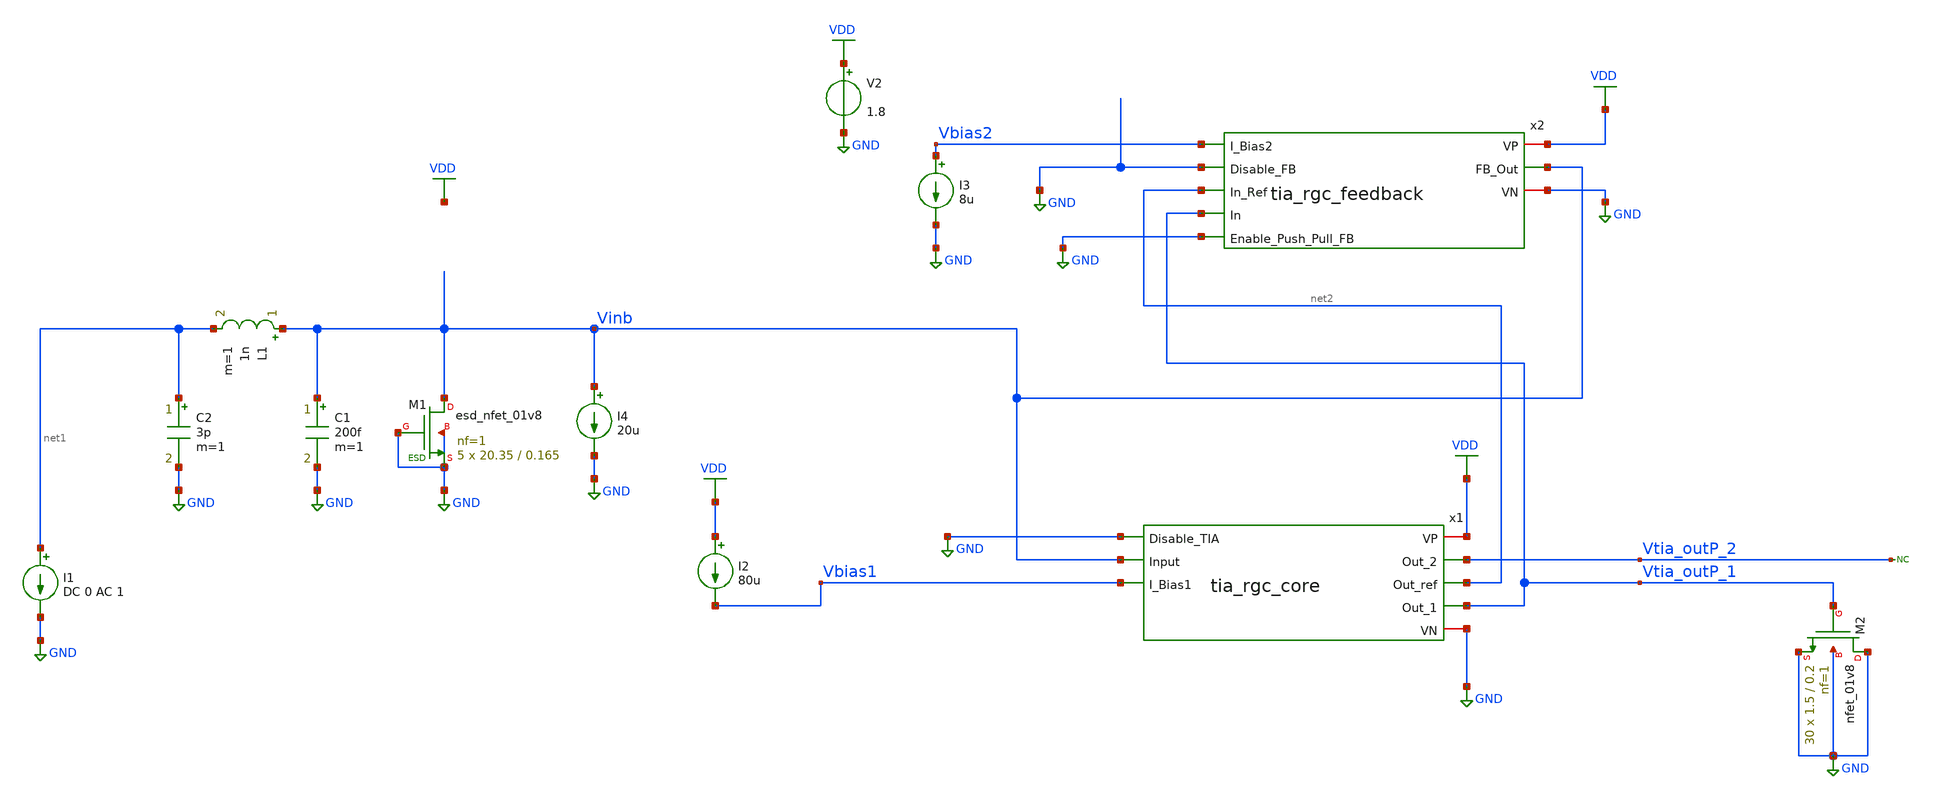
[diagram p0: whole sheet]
** sch_path: xschem/test/test_tia_rgc_full.sch
**.subckt test_tia_rgc_full
V2 VDD GND 1.8
I1 net1 GND DC 0 AC 1
I2 VDD Vbias1 80u
C1 Vinb GND 200f m=1
L1 Vinb net1 1n m=1
C2 net1 GND 3p m=1
XM1 Vinb GND GND GND sky130_fd_pr__esd_nfet_01v8 L=0.165 W=20.35 nf=1 ad='int((nf+1)/2) * W/nf * 0.29'
+ as='int((nf+2)/2) * W/nf * 0.29' pd='2*int((nf+1)/2) * (W/nf + 0.29)' ps='2*int((nf+2)/2) * (W/nf + 0.29)'
+ nrd='0.29 / W' nrs='0.29 / W' sa=0 sb=0 sd=0 mult=5 m=5
I3 Vbias2 GND 8u
XM2 GND Vtia_outP_1 GND GND sky130_fd_pr__nfet_01v8 L=0.2 W=1.5 nf=1 ad='int((nf+1)/2) * W/nf * 0.29'
+ as='int((nf+2)/2) * W/nf * 0.29' pd='2*int((nf+1)/2) * (W/nf + 0.29)' ps='2*int((nf+2)/2) * (W/nf + 0.29)'
+ nrd='0.29 / W' nrs='0.29 / W' sa=0 sb=0 sd=0 mult=30 m=30
x1 VDD Vtia_outP_2 net2 Vtia_outP_1 GND Vinb Vbias1 GND tia_rgc_core
x2 VDD Vbias2 Vinb GND net2 Vtia_outP_1 GND GND tia_rgc_feedback
* noconn Vtia_outP_2
I4 Vinb GND 20u
**** begin user architecture code


*.options savecurrents
.option warn=1
* .option temp=100
.control
set wr_vecnames
set wr_singlescale
set hcopydevtype=svg
** TIA


op
write test_tia_rgc_full.raw
run
reset
* option temp=20
* noise v(Vtia_outP-Vtia_outN) iin dec 100 1 100G
* print all
* setplot noise2
* write noise_tia2.raw
* wrdata result_noise_tia2.csv
* run
* reset

ac dec 1000 10 1T
plot vdb(Vtia_outP_1) vdb(Vtia_outP_2)
plot v(Vinb)
plot phase(Vinb)/pi*180 phase(Vtia_outP_1)/pi*180
hardcopy bandwidth.svg vdb(Vtia_outP_1)
hardcopy impedance.svg v(Vinb)


* tran 1p 100n
* plot v(Vtia_outP_1) v(Vtia_outP_2)
* plot v(Vinb)
meas ac gain FIND vdb(vtia_outp_1) AT=10MEG
meas ac max_gain max vdb(vtia_outp_1) from=1MEG to=100G
meas ac min_gain min vdb(vtia_outp_1) from=1MEG to=100MEG
let bw_gain=gain-3
meas ac bandwidth when vdb(vtia_outp_1)=bw_gain fall = LAST
wrdata result_freq.csv gain max_gain min_gain bandwidth
run
reset
noise v(vtia_outp_1) i1 dec 1000 10 2G
print all
* wrdata result_noise.csv inoise_total onoise_total
setplot noise1
plot inoise_spectrum
plot onoise_spectrum
hardcopy tia_rgc_inoise_spectrum.svg inoise_spectrum
hardcopy tia_rgc_onoise_spectrum.svg onoise_spectrum
* plot log(inoise_spectrum)
* write noise_tia2.raw
run
*
reset
noise v(vtia_outp_1) i1 dec 1000 2MEG 2G
print all
* wrdata result_noise.csv inoise_total onoise_total
setplot noise3
plot inoise_spectrum
plot onoise_spectrum
hardcopy tia_rgc_inoise_spectrum_zoom.svg inoise_spectrum
hardcopy tia_rgc_onoise_spectrum_zoom.svg onoise_spectrum
* plot log(inoise_spectrum)
* write noise_tia2.raw
run
*


.endc




* .include ../../tia.spice
* .include ../../filter_diff.spice
* .include ../../cmm_sense3.spice

.include tia_rgc_core.spice
.include tia_rgc_feedback.spice



* .lib $::SKYWATER_MODELS/sky130.lib.spice #model#
* .lib $::SKYWATER_MODELS/sky130.lib.spice sf
.lib $::SKYWATER_MODELS/sky130.lib.spice.tt.red tt
* .lib /home/simon/share/pdk/sky130A/libs.tech/ngspice/sky130.lib.spice.tt.red tt

**** end user architecture code
**.ends

* expanding   symbol:  /home/simon/code/asic/analog/tia/tia_rgc_core.sym # of pins=8
** sym_path: xschem/tia/tia_rgc_core.sym
** sch_path: xschem/tia/tia_rgc_core.sch
.subckt tia_rgc_core VP Out_2 Out_ref Out_1 Disable_TIA Input I_Bias1 VN
*.iopin VN
*.iopin VP
*.opin Out_2
*.ipin I_Bias1
*.ipin Input
*.ipin Disable_TIA
*.opin Out_1
*.opin Out_ref
XM5 VM5D I_Bias1 VN VN sky130_fd_pr__nfet_01v8 L=1 W=2 nf=1 ad='int((nf+1)/2) * W/nf * 0.29' as='int((nf+2)/2) * W/nf * 0.29'
+ pd='2*int((nf+1)/2) * (W/nf + 0.29)' ps='2*int((nf+2)/2) * (W/nf + 0.29)' nrd='0.29 / W' nrs='0.29 / W'
+ sa=0 sb=0 sd=0 mult=6 m=6
XM6 VM6D I_Bias1 VN VN sky130_fd_pr__nfet_01v8 L=1.0 W=2 nf=1 ad='int((nf+1)/2) * W/nf * 0.29' as='int((nf+2)/2) * W/nf * 0.29'
+ pd='2*int((nf+1)/2) * (W/nf + 0.29)' ps='2*int((nf+2)/2) * (W/nf + 0.29)' nrd='0.29 / W' nrs='0.29 / W'
+ sa=0 sb=0 sd=0 mult=6 m=6
XM7 Out_1 Input VM28D VN sky130_fd_pr__nfet_01v8_lvt L=0.2 W=2 nf=1 ad='int((nf+1)/2) * W/nf * 0.29'
+ as='int((nf+2)/2) * W/nf * 0.29' pd='2*int((nf+1)/2) * (W/nf + 0.29)' ps='2*int((nf+2)/2) * (W/nf + 0.29)'
+ nrd='0.29 / W' nrs='0.29 / W' sa=0 sb=0 sd=0 mult=100 m=100
XM8 Out_1 Input VP VP sky130_fd_pr__pfet_01v8 L=0.2 W=2 nf=1 ad='int((nf+1)/2) * W/nf * 0.29' as='int((nf+2)/2) * W/nf * 0.29'
+ pd='2*int((nf+1)/2) * (W/nf + 0.29)' ps='2*int((nf+2)/2) * (W/nf + 0.29)' nrd='0.29 / W' nrs='0.29 / W'
+ sa=0 sb=0 sd=0 mult=60 m=60
XM9 Input I_Bias1 VM5D VN sky130_fd_pr__nfet_01v8 L=0.15 W=2 nf=1 ad='int((nf+1)/2) * W/nf * 0.29' as='int((nf+2)/2) * W/nf * 0.29'
+ pd='2*int((nf+1)/2) * (W/nf + 0.29)' ps='2*int((nf+2)/2) * (W/nf + 0.29)' nrd='0.29 / W' nrs='0.29 / W'
+ sa=0 sb=0 sd=0 mult=12 m=12
XM10 I_Bias1 I_Bias1 VM6D VN sky130_fd_pr__nfet_01v8 L=0.15 W=2 nf=1 ad='int((nf+1)/2) * W/nf * 0.29'
+ as='int((nf+2)/2) * W/nf * 0.29' pd='2*int((nf+1)/2) * (W/nf + 0.29)' ps='2*int((nf+2)/2) * (W/nf + 0.29)'
+ nrd='0.29 / W' nrs='0.29 / W' sa=0 sb=0 sd=0 mult=12 m=12
XM23 I_Bias1 Disable_TIA VN VN sky130_fd_pr__nfet_01v8 L=0.15 W=2 nf=1 ad='int((nf+1)/2) * W/nf * 0.29'
+ as='int((nf+2)/2) * W/nf * 0.29' pd='2*int((nf+1)/2) * (W/nf + 0.29)' ps='2*int((nf+2)/2) * (W/nf + 0.29)'
+ nrd='0.29 / W' nrs='0.29 / W' sa=0 sb=0 sd=0 mult=5 m=5
XM26 Disable_TIA_B Disable_TIA VN VN sky130_fd_pr__nfet_01v8 L=1 W=0.5 nf=1 ad='int((nf+1)/2) * W/nf * 0.29'
+ as='int((nf+2)/2) * W/nf * 0.29' pd='2*int((nf+1)/2) * (W/nf + 0.29)' ps='2*int((nf+2)/2) * (W/nf + 0.29)'
+ nrd='0.29 / W' nrs='0.29 / W' sa=0 sb=0 sd=0 mult=1 m=1
XM27 Disable_TIA_B Disable_TIA VP VP sky130_fd_pr__pfet_01v8 L=1 W=0.5 nf=1 ad='int((nf+1)/2) * W/nf * 0.29'
+ as='int((nf+2)/2) * W/nf * 0.29' pd='2*int((nf+1)/2) * (W/nf + 0.29)' ps='2*int((nf+2)/2) * (W/nf + 0.29)'
+ nrd='0.29 / W' nrs='0.29 / W' sa=0 sb=0 sd=0 mult=1 m=1
XM28 VM28D Disable_TIA_B VN VN sky130_fd_pr__nfet_01v8 L=0.15 W=2 nf=1 ad='int((nf+1)/2) * W/nf * 0.29'
+ as='int((nf+2)/2) * W/nf * 0.29' pd='2*int((nf+1)/2) * (W/nf + 0.29)' ps='2*int((nf+2)/2) * (W/nf + 0.29)'
+ nrd='0.29 / W' nrs='0.29 / W' sa=0 sb=0 sd=0 mult=100 m=100
XM36 VM36D I_Bias1 VN VN sky130_fd_pr__nfet_01v8 L=1 W=2 nf=1 ad='int((nf+1)/2) * W/nf * 0.29' as='int((nf+2)/2) * W/nf * 0.29'
+ pd='2*int((nf+1)/2) * (W/nf + 0.29)' ps='2*int((nf+2)/2) * (W/nf + 0.29)' nrd='0.29 / W' nrs='0.29 / W'
+ sa=0 sb=0 sd=0 mult=6 m=6
XM37 Out_ref VM39D VM40D VN sky130_fd_pr__nfet_01v8_lvt L=0.2 W=2 nf=1 ad='int((nf+1)/2) * W/nf * 0.29'
+ as='int((nf+2)/2) * W/nf * 0.29' pd='2*int((nf+1)/2) * (W/nf + 0.29)' ps='2*int((nf+2)/2) * (W/nf + 0.29)'
+ nrd='0.29 / W' nrs='0.29 / W' sa=0 sb=0 sd=0 mult=100 m=100
XM38 Out_ref VM39D VP VP sky130_fd_pr__pfet_01v8 L=0.2 W=2 nf=1 ad='int((nf+1)/2) * W/nf * 0.29' as='int((nf+2)/2) * W/nf * 0.29'
+ pd='2*int((nf+1)/2) * (W/nf + 0.29)' ps='2*int((nf+2)/2) * (W/nf + 0.29)' nrd='0.29 / W' nrs='0.29 / W'
+ sa=0 sb=0 sd=0 mult=60 m=60
XM39 VM39D I_Bias1 VM36D VN sky130_fd_pr__nfet_01v8 L=0.15 W=2 nf=1 ad='int((nf+1)/2) * W/nf * 0.29'
+ as='int((nf+2)/2) * W/nf * 0.29' pd='2*int((nf+1)/2) * (W/nf + 0.29)' ps='2*int((nf+2)/2) * (W/nf + 0.29)'
+ nrd='0.29 / W' nrs='0.29 / W' sa=0 sb=0 sd=0 mult=12 m=12
XM40 VM40D Disable_TIA_B VN VN sky130_fd_pr__nfet_01v8 L=0.15 W=2 nf=1 ad='int((nf+1)/2) * W/nf * 0.29'
+ as='int((nf+2)/2) * W/nf * 0.29' pd='2*int((nf+1)/2) * (W/nf + 0.29)' ps='2*int((nf+2)/2) * (W/nf + 0.29)'
+ nrd='0.29 / W' nrs='0.29 / W' sa=0 sb=0 sd=0 mult=100 m=100
XC20 VP VN sky130_fd_pr__cap_mim_m3_2 W=30 L=30 MF=1 m=1
XM16 Out_2 VN VP VP sky130_fd_pr__pfet_01v8 L=0.5 W=2 nf=1 ad='int((nf+1)/2) * W/nf * 0.29' as='int((nf+2)/2) * W/nf * 0.29'
+ pd='2*int((nf+1)/2) * (W/nf + 0.29)' ps='2*int((nf+2)/2) * (W/nf + 0.29)' nrd='0.29 / W' nrs='0.29 / W'
+ sa=0 sb=0 sd=0 mult=10 m=10
XM15 Out_2 Out_1 Input Input sky130_fd_pr__nfet_01v8_lvt L=0.2 W=2 nf=1 ad='int((nf+1)/2) * W/nf * 0.29'
+ as='int((nf+2)/2) * W/nf * 0.29' pd='2*int((nf+1)/2) * (W/nf + 0.29)' ps='2*int((nf+2)/2) * (W/nf + 0.29)'
+ nrd='0.29 / W' nrs='0.29 / W' sa=0 sb=0 sd=0 mult=30 m=30
XM31 VM31D Out_ref VM39D VM39D sky130_fd_pr__nfet_01v8_lvt L=0.2 W=2 nf=1 ad='int((nf+1)/2) * W/nf * 0.29'
+ as='int((nf+2)/2) * W/nf * 0.29' pd='2*int((nf+1)/2) * (W/nf + 0.29)' ps='2*int((nf+2)/2) * (W/nf + 0.29)'
+ nrd='0.29 / W' nrs='0.29 / W' sa=0 sb=0 sd=0 mult=30 m=30
XM35 VM31D VN VP VP sky130_fd_pr__pfet_01v8 L=0.5 W=2 nf=1 ad='int((nf+1)/2) * W/nf * 0.29' as='int((nf+2)/2) * W/nf * 0.29'
+ pd='2*int((nf+1)/2) * (W/nf + 0.29)' ps='2*int((nf+2)/2) * (W/nf + 0.29)' nrd='0.29 / W' nrs='0.29 / W'
+ sa=0 sb=0 sd=0 mult=10 m=10
XC7 VP VN sky130_fd_pr__cap_mim_m3_2 W=30 L=30 MF=1 m=1
XC2 VP VM28D sky130_fd_pr__cap_mim_m3_2 W=20 L=30 MF=1 m=1
XC5 VN I_Bias1 sky130_fd_pr__cap_mim_m3_1 W=15 L=12 MF=1 m=1
XC4 VN I_Bias1 sky130_fd_pr__cap_mim_m3_1 W=15 L=12 MF=1 m=1
XC1 VP VM40D sky130_fd_pr__cap_mim_m3_2 W=20 L=30 MF=1 m=1
XC3 Disable_TIA_B VN VN sky130_fd_pr__cap_var_lvt W=2 L=5 VM=5 m=5
.ends


* expanding   symbol:  /home/simon/code/asic/analog/tia/tia_rgc_feedback.sym # of pins=8
** sym_path: xschem/tia/tia_rgc_feedback.sym
** sch_path: xschem/tia/tia_rgc_feedback.sch
.subckt tia_rgc_feedback VP I_Bias2 FB_Out Disable_FB In_Ref In Enable_Push_Pull_FB VN
*.iopin VN
*.iopin VP
*.ipin I_Bias2
*.ipin Disable_FB
*.ipin Enable_Push_Pull_FB
*.ipin In_Ref
*.opin FB_Out
*.ipin In
XM3 net2 net1 VN VN sky130_fd_pr__nfet_01v8 L=0.5 W=2 nf=1 ad='int((nf+1)/2) * W/nf * 0.29' as='int((nf+2)/2) * W/nf * 0.29'
+ pd='2*int((nf+1)/2) * (W/nf + 0.29)' ps='2*int((nf+2)/2) * (W/nf + 0.29)' nrd='0.29 / W' nrs='0.29 / W'
+ sa=0 sb=0 sd=0 mult=1 m=1
XM4 net1 net1 net2 VN sky130_fd_pr__nfet_01v8 L=0.15 W=2 nf=1 ad='int((nf+1)/2) * W/nf * 0.29' as='int((nf+2)/2) * W/nf * 0.29'
+ pd='2*int((nf+1)/2) * (W/nf + 0.29)' ps='2*int((nf+2)/2) * (W/nf + 0.29)' nrd='0.29 / W' nrs='0.29 / W'
+ sa=0 sb=0 sd=0 mult=4 m=4
XM12 net3 net1 VN VN sky130_fd_pr__nfet_01v8 L=0.5 W=2 nf=1 ad='int((nf+1)/2) * W/nf * 0.29' as='int((nf+2)/2) * W/nf * 0.29'
+ pd='2*int((nf+1)/2) * (W/nf + 0.29)' ps='2*int((nf+2)/2) * (W/nf + 0.29)' nrd='0.29 / W' nrs='0.29 / W'
+ sa=0 sb=0 sd=0 mult=2 m=2
XM13 VM13D net1 net3 VN sky130_fd_pr__nfet_01v8 L=0.15 W=2 nf=1 ad='int((nf+1)/2) * W/nf * 0.29' as='int((nf+2)/2) * W/nf * 0.29'
+ pd='2*int((nf+1)/2) * (W/nf + 0.29)' ps='2*int((nf+2)/2) * (W/nf + 0.29)' nrd='0.29 / W' nrs='0.29 / W'
+ sa=0 sb=0 sd=0 mult=8 m=8
XM1 net5 I_Bias2 VP VP sky130_fd_pr__pfet_01v8 L=0.5 W=2 nf=1 ad='int((nf+1)/2) * W/nf * 0.29' as='int((nf+2)/2) * W/nf * 0.29'
+ pd='2*int((nf+1)/2) * (W/nf + 0.29)' ps='2*int((nf+2)/2) * (W/nf + 0.29)' nrd='0.29 / W' nrs='0.29 / W'
+ sa=0 sb=0 sd=0 mult=2 m=2
XM29 Disable_FB_B Disable_FB VN VN sky130_fd_pr__nfet_01v8 L=0.15 W=1 nf=1 ad='int((nf+1)/2) * W/nf * 0.29'
+ as='int((nf+2)/2) * W/nf * 0.29' pd='2*int((nf+1)/2) * (W/nf + 0.29)' ps='2*int((nf+2)/2) * (W/nf + 0.29)'
+ nrd='0.29 / W' nrs='0.29 / W' sa=0 sb=0 sd=0 mult=1 m=1
XM30 Disable_FB_B Disable_FB VP VP sky130_fd_pr__pfet_01v8 L=0.15 W=1 nf=1 ad='int((nf+1)/2) * W/nf * 0.29'
+ as='int((nf+2)/2) * W/nf * 0.29' pd='2*int((nf+1)/2) * (W/nf + 0.29)' ps='2*int((nf+2)/2) * (W/nf + 0.29)'
+ nrd='0.29 / W' nrs='0.29 / W' sa=0 sb=0 sd=0 mult=1 m=1
XM32 VM14D Disable_FB_B VP VP sky130_fd_pr__pfet_01v8 L=0.15 W=2 nf=1 ad='int((nf+1)/2) * W/nf * 0.29'
+ as='int((nf+2)/2) * W/nf * 0.29' pd='2*int((nf+1)/2) * (W/nf + 0.29)' ps='2*int((nf+2)/2) * (W/nf + 0.29)'
+ nrd='0.29 / W' nrs='0.29 / W' sa=0 sb=0 sd=0 mult=1 m=1
XM33 VM16D Disable_FB_B VP VP sky130_fd_pr__pfet_01v8 L=0.15 W=2 nf=1 ad='int((nf+1)/2) * W/nf * 0.29'
+ as='int((nf+2)/2) * W/nf * 0.29' pd='2*int((nf+1)/2) * (W/nf + 0.29)' ps='2*int((nf+2)/2) * (W/nf + 0.29)'
+ nrd='0.29 / W' nrs='0.29 / W' sa=0 sb=0 sd=0 mult=1 m=1
XM42 net4 net1 VN VN sky130_fd_pr__nfet_01v8 L=0.5 W=2 nf=1 ad='int((nf+1)/2) * W/nf * 0.29' as='int((nf+2)/2) * W/nf * 0.29'
+ pd='2*int((nf+1)/2) * (W/nf + 0.29)' ps='2*int((nf+2)/2) * (W/nf + 0.29)' nrd='0.29 / W' nrs='0.29 / W'
+ sa=0 sb=0 sd=0 mult=1 m=1
XM43 VM34G net1 net4 VN sky130_fd_pr__nfet_01v8 L=0.15 W=2 nf=1 ad='int((nf+1)/2) * W/nf * 0.29' as='int((nf+2)/2) * W/nf * 0.29'
+ pd='2*int((nf+1)/2) * (W/nf + 0.29)' ps='2*int((nf+2)/2) * (W/nf + 0.29)' nrd='0.29 / W' nrs='0.29 / W'
+ sa=0 sb=0 sd=0 mult=4 m=4
XM17 net1 I_Bias2 net5 VP sky130_fd_pr__pfet_01v8 L=0.15 W=2 nf=1 ad='int((nf+1)/2) * W/nf * 0.29' as='int((nf+2)/2) * W/nf * 0.29'
+ pd='2*int((nf+1)/2) * (W/nf + 0.29)' ps='2*int((nf+2)/2) * (W/nf + 0.29)' nrd='0.29 / W' nrs='0.29 / W'
+ sa=0 sb=0 sd=0 mult=8 m=8
XM2 net6 I_Bias2 VP VP sky130_fd_pr__pfet_01v8 L=0.5 W=2 nf=1 ad='int((nf+1)/2) * W/nf * 0.29' as='int((nf+2)/2) * W/nf * 0.29'
+ pd='2*int((nf+1)/2) * (W/nf + 0.29)' ps='2*int((nf+2)/2) * (W/nf + 0.29)' nrd='0.29 / W' nrs='0.29 / W'
+ sa=0 sb=0 sd=0 mult=2 m=2
XM18 VM16D I_Bias2 net6 VP sky130_fd_pr__pfet_01v8 L=0.15 W=2 nf=1 ad='int((nf+1)/2) * W/nf * 0.29' as='int((nf+2)/2) * W/nf * 0.29'
+ pd='2*int((nf+1)/2) * (W/nf + 0.29)' ps='2*int((nf+2)/2) * (W/nf + 0.29)' nrd='0.29 / W' nrs='0.29 / W'
+ sa=0 sb=0 sd=0 mult=8 m=8
XM19 net7 I_Bias2 VP VP sky130_fd_pr__pfet_01v8 L=0.5 W=2 nf=1 ad='int((nf+1)/2) * W/nf * 0.29' as='int((nf+2)/2) * W/nf * 0.29'
+ pd='2*int((nf+1)/2) * (W/nf + 0.29)' ps='2*int((nf+2)/2) * (W/nf + 0.29)' nrd='0.29 / W' nrs='0.29 / W'
+ sa=0 sb=0 sd=0 mult=2 m=2
XM20 VM14D I_Bias2 net7 VP sky130_fd_pr__pfet_01v8 L=0.15 W=2 nf=1 ad='int((nf+1)/2) * W/nf * 0.29' as='int((nf+2)/2) * W/nf * 0.29'
+ pd='2*int((nf+1)/2) * (W/nf + 0.29)' ps='2*int((nf+2)/2) * (W/nf + 0.29)' nrd='0.29 / W' nrs='0.29 / W'
+ sa=0 sb=0 sd=0 mult=8 m=8
XM34 FB_Out VM34G net10 VN sky130_fd_pr__nfet_01v8 L=0.15 W=2 nf=1 ad='int((nf+1)/2) * W/nf * 0.29' as='int((nf+2)/2) * W/nf * 0.29'
+ pd='2*int((nf+1)/2) * (W/nf + 0.29)' ps='2*int((nf+2)/2) * (W/nf + 0.29)' nrd='0.29 / W' nrs='0.29 / W'
+ sa=0 sb=0 sd=0 mult=10 m=10
XM25 FB_Out VM25G net11 VP sky130_fd_pr__pfet_01v8 L=0.15 W=2 nf=1 ad='int((nf+1)/2) * W/nf * 0.29' as='int((nf+2)/2) * W/nf * 0.29'
+ pd='2*int((nf+1)/2) * (W/nf + 0.29)' ps='2*int((nf+2)/2) * (W/nf + 0.29)' nrd='0.29 / W' nrs='0.29 / W'
+ sa=0 sb=0 sd=0 mult=20 m=20
XM45 VM25G VM25G net8 net8 sky130_fd_pr__nfet_01v8_lvt L=0.15 W=1 nf=1 ad='int((nf+1)/2) * W/nf * 0.29'
+ as='int((nf+2)/2) * W/nf * 0.29' pd='2*int((nf+1)/2) * (W/nf + 0.29)' ps='2*int((nf+2)/2) * (W/nf + 0.29)'
+ nrd='0.29 / W' nrs='0.29 / W' sa=0 sb=0 sd=0 mult=1 m=1
XM46 FB_Out VM14D VP VP sky130_fd_pr__pfet_01v8 L=0.3 W=2 nf=1 ad='int((nf+1)/2) * W/nf * 0.29' as='int((nf+2)/2) * W/nf * 0.29'
+ pd='2*int((nf+1)/2) * (W/nf + 0.29)' ps='2*int((nf+2)/2) * (W/nf + 0.29)' nrd='0.29 / W' nrs='0.29 / W'
+ sa=0 sb=0 sd=0 mult=3 m=3
XM47 net9 net1 VN VN sky130_fd_pr__nfet_01v8 L=0.5 W=2 nf=1 ad='int((nf+1)/2) * W/nf * 0.29' as='int((nf+2)/2) * W/nf * 0.29'
+ pd='2*int((nf+1)/2) * (W/nf + 0.29)' ps='2*int((nf+2)/2) * (W/nf + 0.29)' nrd='0.29 / W' nrs='0.29 / W'
+ sa=0 sb=0 sd=0 mult=3 m=3
XM48 FB_Out net1 net9 VN sky130_fd_pr__nfet_01v8 L=0.15 W=2 nf=1 ad='int((nf+1)/2) * W/nf * 0.29' as='int((nf+2)/2) * W/nf * 0.29'
+ pd='2*int((nf+1)/2) * (W/nf + 0.29)' ps='2*int((nf+2)/2) * (W/nf + 0.29)' nrd='0.29 / W' nrs='0.29 / W'
+ sa=0 sb=0 sd=0 mult=12 m=12
XC8 VP VM14D sky130_fd_pr__cap_mim_m3_2 W=20 L=20 MF=1 m=1
XM52 EN_PP_FB Enable_Push_Pull_FB VN VN sky130_fd_pr__nfet_01v8 L=0.15 W=1 nf=1 ad='int((nf+1)/2) * W/nf * 0.29'
+ as='int((nf+2)/2) * W/nf * 0.29' pd='2*int((nf+1)/2) * (W/nf + 0.29)' ps='2*int((nf+2)/2) * (W/nf + 0.29)'
+ nrd='0.29 / W' nrs='0.29 / W' sa=0 sb=0 sd=0 mult=1 m=1
XM53 EN_PP_FB Enable_Push_Pull_FB VP VP sky130_fd_pr__pfet_01v8 L=0.15 W=1 nf=1 ad='int((nf+1)/2) * W/nf * 0.29'
+ as='int((nf+2)/2) * W/nf * 0.29' pd='2*int((nf+1)/2) * (W/nf + 0.29)' ps='2*int((nf+2)/2) * (W/nf + 0.29)'
+ nrd='0.29 / W' nrs='0.29 / W' sa=0 sb=0 sd=0 mult=1 m=1
XM49 net8 Enable_Push_Pull_FB VM34G VN sky130_fd_pr__nfet_01v8_lvt L=0.15 W=1 nf=1 ad='int((nf+1)/2) * W/nf * 0.29'
+ as='int((nf+2)/2) * W/nf * 0.29' pd='2*int((nf+1)/2) * (W/nf + 0.29)' ps='2*int((nf+2)/2) * (W/nf + 0.29)'
+ nrd='0.29 / W' nrs='0.29 / W' sa=0 sb=0 sd=0 mult=1 m=1
XM50 VM34G EN_PP_FB VN VN sky130_fd_pr__nfet_01v8_lvt L=0.15 W=1 nf=1 ad='int((nf+1)/2) * W/nf * 0.29'
+ as='int((nf+2)/2) * W/nf * 0.29' pd='2*int((nf+1)/2) * (W/nf + 0.29)' ps='2*int((nf+2)/2) * (W/nf + 0.29)'
+ nrd='0.29 / W' nrs='0.29 / W' sa=0 sb=0 sd=0 mult=1 m=1
XM51 VM25G Enable_Push_Pull_FB VP VP sky130_fd_pr__pfet_01v8 L=0.15 W=1 nf=1 ad='int((nf+1)/2) * W/nf * 0.29'
+ as='int((nf+2)/2) * W/nf * 0.29' pd='2*int((nf+1)/2) * (W/nf + 0.29)' ps='2*int((nf+2)/2) * (W/nf + 0.29)'
+ nrd='0.29 / W' nrs='0.29 / W' sa=0 sb=0 sd=0 mult=1 m=1
XM44 net10 VM34G VN VN sky130_fd_pr__nfet_01v8 L=0.5 W=2 nf=1 ad='int((nf+1)/2) * W/nf * 0.29' as='int((nf+2)/2) * W/nf * 0.29'
+ pd='2*int((nf+1)/2) * (W/nf + 0.29)' ps='2*int((nf+2)/2) * (W/nf + 0.29)' nrd='0.29 / W' nrs='0.29 / W'
+ sa=0 sb=0 sd=0 mult=5 m=5
XM54 net11 VM25G VP VP sky130_fd_pr__pfet_01v8 L=0.5 W=2 nf=1 ad='int((nf+1)/2) * W/nf * 0.29' as='int((nf+2)/2) * W/nf * 0.29'
+ pd='2*int((nf+1)/2) * (W/nf + 0.29)' ps='2*int((nf+2)/2) * (W/nf + 0.29)' nrd='0.29 / W' nrs='0.29 / W'
+ sa=0 sb=0 sd=0 mult=10 m=10
XM11 VM25G VM16D VP VP sky130_fd_pr__pfet_01v8_lvt L=0.35 W=2 nf=1 ad='int((nf+1)/2) * W/nf * 0.29' as='int((nf+2)/2) * W/nf * 0.29'
+ pd='2*int((nf+1)/2) * (W/nf + 0.29)' ps='2*int((nf+2)/2) * (W/nf + 0.29)' nrd='0.29 / W' nrs='0.29 / W'
+ sa=0 sb=0 sd=0 mult=2 m=2
XC20 VP VN sky130_fd_pr__cap_mim_m3_2 W=30 L=30 MF=1 m=1
XC18 net1 VN VN sky130_fd_pr__cap_var_lvt W=3 L=3 VM=10 m=10
XC11 VM16D VN VN sky130_fd_pr__cap_var_lvt W=3 L=3 VM=20 m=20
XC12 VP VM16D sky130_fd_pr__cap_mim_m3_2 W=20 L=20 MF=1 m=1
XC22 Enable_Push_Pull_FB VN sky130_fd_pr__cap_mim_m3_2 W=20 L=20 MF=1 m=1
XM21 net12 I_Bias2 VP VP sky130_fd_pr__pfet_01v8 L=0.5 W=2 nf=1 ad='int((nf+1)/2) * W/nf * 0.29' as='int((nf+2)/2) * W/nf * 0.29'
+ pd='2*int((nf+1)/2) * (W/nf + 0.29)' ps='2*int((nf+2)/2) * (W/nf + 0.29)' nrd='0.29 / W' nrs='0.29 / W'
+ sa=0 sb=0 sd=0 mult=2 m=2
XM22 I_Bias2 I_Bias2 net12 VP sky130_fd_pr__pfet_01v8 L=0.15 W=2 nf=1 ad='int((nf+1)/2) * W/nf * 0.29'
+ as='int((nf+2)/2) * W/nf * 0.29' pd='2*int((nf+1)/2) * (W/nf + 0.29)' ps='2*int((nf+2)/2) * (W/nf + 0.29)'
+ nrd='0.29 / W' nrs='0.29 / W' sa=0 sb=0 sd=0 mult=8 m=8
XM55 net1 Disable_FB VN VN sky130_fd_pr__nfet_01v8_lvt L=0.15 W=1 nf=1 ad='int((nf+1)/2) * W/nf * 0.29'
+ as='int((nf+2)/2) * W/nf * 0.29' pd='2*int((nf+1)/2) * (W/nf + 0.29)' ps='2*int((nf+2)/2) * (W/nf + 0.29)'
+ nrd='0.29 / W' nrs='0.29 / W' sa=0 sb=0 sd=0 mult=1 m=1
XM24 VM16D In_Ref VM13D VM13D sky130_fd_pr__nfet_01v8_lvt L=0.5 W=2 nf=1 ad='int((nf+1)/2) * W/nf * 0.29'
+ as='int((nf+2)/2) * W/nf * 0.29' pd='2*int((nf+1)/2) * (W/nf + 0.29)' ps='2*int((nf+2)/2) * (W/nf + 0.29)'
+ nrd='0.29 / W' nrs='0.29 / W' sa=0 sb=0 sd=0 mult=2 m=2
XM14 VM14D In VM13D VM13D sky130_fd_pr__nfet_01v8_lvt L=0.5 W=2 nf=1 ad='int((nf+1)/2) * W/nf * 0.29'
+ as='int((nf+2)/2) * W/nf * 0.29' pd='2*int((nf+1)/2) * (W/nf + 0.29)' ps='2*int((nf+2)/2) * (W/nf + 0.29)'
+ nrd='0.29 / W' nrs='0.29 / W' sa=0 sb=0 sd=0 mult=2 m=2
XC13 VM14D VN VN sky130_fd_pr__cap_var_lvt W=3 L=3 VM=20 m=20
XC1 VN VP sky130_fd_pr__cap_mim_m3_2 W=30 L=30 MF=1 m=1
XC2 Enable_Push_Pull_FB VN VN sky130_fd_pr__cap_var_lvt W=3 L=3 VM=10 m=10
XC3 net1 VN sky130_fd_pr__cap_mim_m3_2 W=20 L=20 MF=1 m=1
.ends

.GLOBAL VDD
.GLOBAL GND
.end
